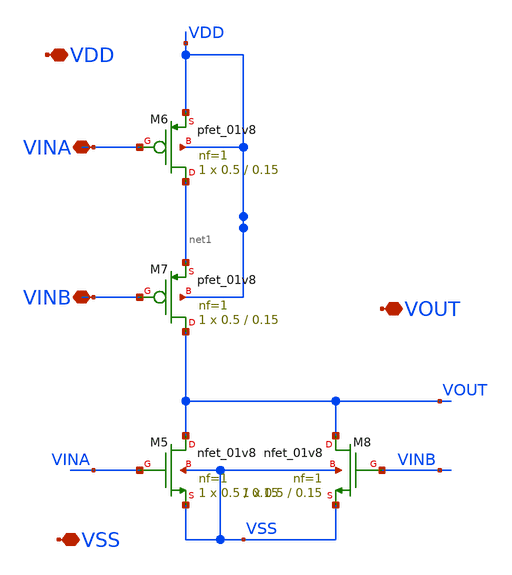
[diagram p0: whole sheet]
** sch_path: xschem/DC_DC_Converter_xschem/OTHERS/DC_DC_Converter_JV11/Delay_block_revised/NOR.sch
**.subckt NOR VDD VSS VINB VINA VOUT
*.iopin VDD
*.iopin VSS
*.iopin VINB
*.iopin VINA
*.iopin VOUT
XM5 VOUT VINA VSS VSS sky130_fd_pr__nfet_01v8 L=0.15 W=0.5 nf=1 ad='int((nf+1)/2) * W/nf * 0.29' as='int((nf+2)/2) * W/nf * 0.29'
+ pd='2*int((nf+1)/2) * (W/nf + 0.29)' ps='2*int((nf+2)/2) * (W/nf + 0.29)' nrd='0.29 / W' nrs='0.29 / W'
+ sa=0 sb=0 sd=0 mult=1 m=1
XM6 net1 VINA VDD VDD sky130_fd_pr__pfet_01v8 L=0.15 W=0.5 nf=1 ad='int((nf+1)/2) * W/nf * 0.29' as='int((nf+2)/2) * W/nf * 0.29'
+ pd='2*int((nf+1)/2) * (W/nf + 0.29)' ps='2*int((nf+2)/2) * (W/nf + 0.29)' nrd='0.29 / W' nrs='0.29 / W'
+ sa=0 sb=0 sd=0 mult=1 m=1
XM7 VOUT VINB net1 VDD sky130_fd_pr__pfet_01v8 L=0.15 W=0.5 nf=1 ad='int((nf+1)/2) * W/nf * 0.29' as='int((nf+2)/2) * W/nf * 0.29'
+ pd='2*int((nf+1)/2) * (W/nf + 0.29)' ps='2*int((nf+2)/2) * (W/nf + 0.29)' nrd='0.29 / W' nrs='0.29 / W'
+ sa=0 sb=0 sd=0 mult=1 m=1
XM8 VOUT VINB VSS VSS sky130_fd_pr__nfet_01v8 L=0.15 W=0.5 nf=1 ad='int((nf+1)/2) * W/nf * 0.29' as='int((nf+2)/2) * W/nf * 0.29'
+ pd='2*int((nf+1)/2) * (W/nf + 0.29)' ps='2*int((nf+2)/2) * (W/nf + 0.29)' nrd='0.29 / W' nrs='0.29 / W'
+ sa=0 sb=0 sd=0 mult=1 m=1
**.ends
.end
